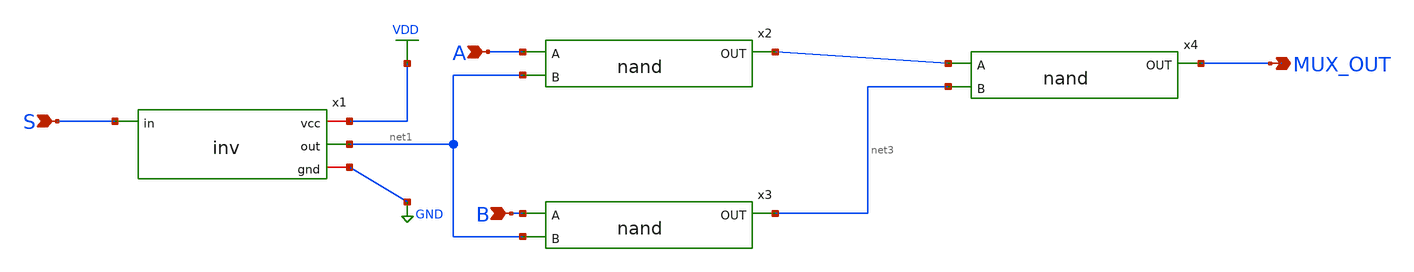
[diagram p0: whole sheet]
** sch_path: designs/schematics/mux2x1/mux_nand.sch
**.subckt mux_nand S A B MUX_OUT
*.ipin S
*.ipin A
*.ipin B
*.opin MUX_OUT
x1 VDD S net1 GND inv
x2 A net1 net2 nand
x3 B net1 net3 nand
x4 net2 net3 MUX_OUT nand
**.ends

* expanding   symbol:  voidwalkers-scandff-gf180mcu/designs/schematics/mux2x1/inv.sym # of pins=4
** sym_path: designs/schematics/mux2x1/inv.sym
** sch_path: designs/schematics/mux2x1/inv.sch
.subckt inv vcc in out gnd
*.ipin in
*.opin out
*.iopin vcc
*.iopin gnd
XM2 out in vcc vcc pfet_03v3 L=0.28u W=0.22u nf=1 ad='int((nf+1)/2) * W/nf * 0.18u' as='int((nf+2)/2) * W/nf * 0.18u'
+ pd='2*int((nf+1)/2) * (W/nf + 0.18u)' ps='2*int((nf+2)/2) * (W/nf + 0.18u)' nrd='0.18u / W' nrs='0.18u / W'
+ sa=0 sb=0 sd=0 m=1
XM1 out in gnd gnd nfet_03v3 L=0.28u W=0.22u nf=1 ad='int((nf+1)/2) * W/nf * 0.18u' as='int((nf+2)/2) * W/nf * 0.18u'
+ pd='2*int((nf+1)/2) * (W/nf + 0.18u)' ps='2*int((nf+2)/2) * (W/nf + 0.18u)' nrd='0.18u / W' nrs='0.18u / W'
+ sa=0 sb=0 sd=0 m=1
.ends


* expanding   symbol:  voidwalkers-scandff-gf180mcu/designs/schematics/mux2x1/nand.sym # of pins=3
** sym_path: designs/schematics/mux2x1/nand.sym
** sch_path: designs/schematics/mux2x1/nand.sch
.subckt nand A B OUT
*.ipin B
*.ipin A
*.opin OUT
XM1 OUT A net1 GND nfet_03v3 L=0.28u W=0.22u nf=1 ad='int((nf+1)/2) * W/nf * 0.18u' as='int((nf+2)/2) * W/nf * 0.18u'
+ pd='2*int((nf+1)/2) * (W/nf + 0.18u)' ps='2*int((nf+2)/2) * (W/nf + 0.18u)' nrd='0.18u / W' nrs='0.18u / W'
+ sa=0 sb=0 sd=0 m=1
XM2 net1 B GND GND nfet_03v3 L=0.28u W=0.22u nf=1 ad='int((nf+1)/2) * W/nf * 0.18u' as='int((nf+2)/2) * W/nf * 0.18u'
+ pd='2*int((nf+1)/2) * (W/nf + 0.18u)' ps='2*int((nf+2)/2) * (W/nf + 0.18u)' nrd='0.18u / W' nrs='0.18u / W'
+ sa=0 sb=0 sd=0 m=1
XM3 OUT A VDD VDD pfet_03v3 L=0.28u W=0.22u nf=1 ad='int((nf+1)/2) * W/nf * 0.18u' as='int((nf+2)/2) * W/nf * 0.18u'
+ pd='2*int((nf+1)/2) * (W/nf + 0.18u)' ps='2*int((nf+2)/2) * (W/nf + 0.18u)' nrd='0.18u / W' nrs='0.18u / W'
+ sa=0 sb=0 sd=0 m=1
XM4 OUT B VDD VDD pfet_03v3 L=0.28u W=0.22u nf=1 ad='int((nf+1)/2) * W/nf * 0.18u' as='int((nf+2)/2) * W/nf * 0.18u'
+ pd='2*int((nf+1)/2) * (W/nf + 0.18u)' ps='2*int((nf+2)/2) * (W/nf + 0.18u)' nrd='0.18u / W' nrs='0.18u / W'
+ sa=0 sb=0 sd=0 m=1
.ends

.GLOBAL VDD
.GLOBAL GND
.end
